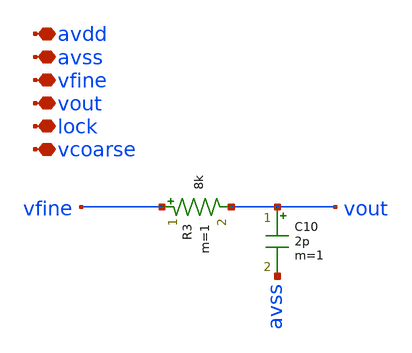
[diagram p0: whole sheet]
** sch_path: xschem/voltage_control.sch
**.subckt voltage_control avdd avss vfine vout lock vcoarse
*.iopin avdd
*.iopin avss
*.iopin vfine
*.iopin vout
*.iopin lock
*.iopin vcoarse
C10 vout avss 2p m=1
R3 vfine vout 8k m=1
**.ends
.end
